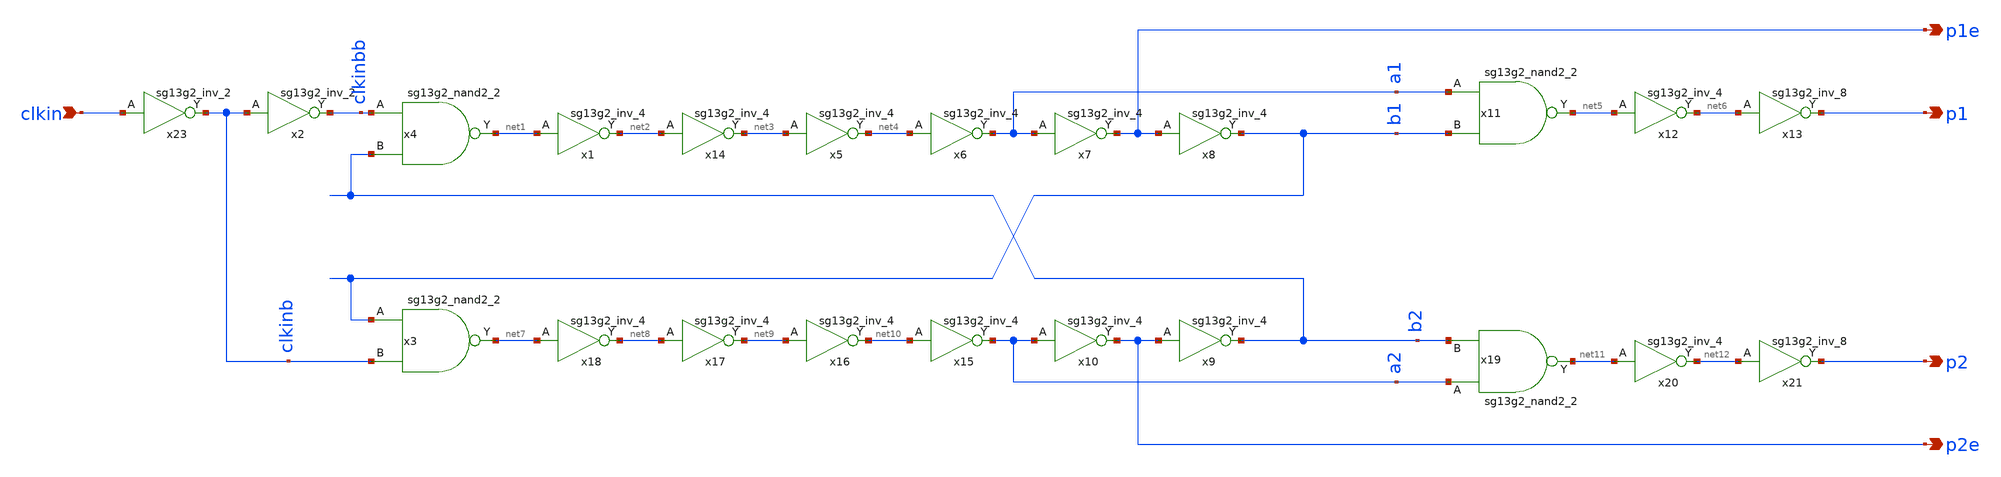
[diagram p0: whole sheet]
** sch_path: 5_Design/4_Layout/Team 6/xschem/clkgen_T6.sch
* IHP-GmbH/IHP-Open-PDK/ihp-sg13g2/libs.tech/xschem/sg13g2_stdcells/sg13g2_inv_2.sch:
* Copyright 2023 IHP PDK Authors
* Licensed under the Apache License, Version 2.0 (the "License");
**.subckt clkgen_T6 clkin p1e p1 p2 p2e
*.ipin clkin
*.opin p1e
*.opin p1
*.opin p2
*.opin p2e
x23 clkinb clkin VDD VSS sg13g2_inv_2
x2 clkinbb clkinb VDD VSS sg13g2_inv_2
x3 net7 b1 clkinb VDD VSS sg13g2_nand2_2
x4 net1 clkinbb b2 VDD VSS sg13g2_nand2_2
x14 net3 net2 VDD VSS sg13g2_inv_4
x1 net2 net1 VDD VSS sg13g2_inv_4
x5 net4 net3 VDD VSS sg13g2_inv_4
x6 a1 net4 VDD VSS sg13g2_inv_4
x7 p1e a1 VDD VSS sg13g2_inv_4
x8 b1 p1e VDD VSS sg13g2_inv_4
x9 b2 p2e VDD VSS sg13g2_inv_4
x10 p2e a2 VDD VSS sg13g2_inv_4
x15 a2 net10 VDD VSS sg13g2_inv_4
x16 net10 net9 VDD VSS sg13g2_inv_4
x17 net9 net8 VDD VSS sg13g2_inv_4
x18 net8 net7 VDD VSS sg13g2_inv_4
x11 net5 a1 b1 VDD VSS sg13g2_nand2_2
x19 net11 a2 b2 VDD VSS sg13g2_nand2_2
x12 net6 net5 VDD VSS sg13g2_inv_4
x20 net12 net11 VDD VSS sg13g2_inv_4
x13 p1 net6 VDD VSS sg13g2_inv_8
x21 p2 net12 VDD VSS sg13g2_inv_8
**.ends

* expanding   symbol:  sg13g2_stdcells/sg13g2_inv_2.sym # of pins=2
** sym_path: sg13g2_stdcells/sg13g2_inv_2.sym
** sch_path: sg13g2_stdcells/sg13g2_inv_2.sch
.subckt sg13g2_inv_2 Y A VDD VSS
*.opin Y
*.ipin A
*.iopin VDD
*.iopin VSS
XM1 Y A VSS VSS sg13_lv_nmos w=1.48u l=130.00n ng=2 m=1 mm_ok=1
XM2 Y A VDD VDD sg13_lv_pmos w=2.24u l=130.00n ng=2 m=1 mm_ok=1
.ends


* expanding   symbol:  sg13g2_stdcells/sg13g2_nand2_2.sym # of pins=3
** sym_path: sg13g2_stdcells/sg13g2_nand2_2.sym
** sch_path: sg13g2_stdcells/sg13g2_nand2_2.sch
.subckt sg13g2_nand2_2 Y A B VDD VSS
*.iopin VDD
*.iopin VSS
*.opin Y
*.ipin B
*.ipin A
XM1 Y A net1 VSS sg13_lv_nmos w=1.44u l=130.00n ng=2 m=1 mm_ok=1
XM2 net1 B VSS VSS sg13_lv_nmos w=1.44u l=130.00n ng=2 m=1 mm_ok=1
XM3 Y A VDD VDD sg13_lv_pmos w=2.24u l=130.00n ng=2 m=1 mm_ok=1
XM4 Y B VDD VDD sg13_lv_pmos w=2.24u l=130.00n ng=2 m=1 mm_ok=1
.ends


* expanding   symbol:  sg13g2_stdcells/sg13g2_inv_4.sym # of pins=2
** sym_path: sg13g2_stdcells/sg13g2_inv_4.sym
** sch_path: sg13g2_stdcells/sg13g2_inv_4.sch
.subckt sg13g2_inv_4 Y A VDD VSS
*.ipin A
*.opin Y
*.iopin VDD
*.iopin VSS
XM1 Y A VSS VSS sg13_lv_nmos w=2.96u l=130.00n ng=4 m=1 mm_ok=1
XM2 Y A VDD VDD sg13_lv_pmos w=4.48u l=130.00n ng=4 m=1 mm_ok=1
.ends


* expanding   symbol:  sg13g2_stdcells/sg13g2_inv_8.sym # of pins=2
** sym_path: sg13g2_stdcells/sg13g2_inv_8.sym
** sch_path: sg13g2_stdcells/sg13g2_inv_8.sch
.subckt sg13g2_inv_8 Y A VDD VSS
*.opin Y
*.ipin A
*.iopin VDD
*.iopin VSS
XM1 Y A VSS VSS sg13_lv_nmos w=5.92u l=130.00n ng=8 m=1 mm_ok=1
XM2 Y A VDD VDD sg13_lv_pmos w=8.96u l=130.00n ng=8 m=1 mm_ok=1
.ends

.end
